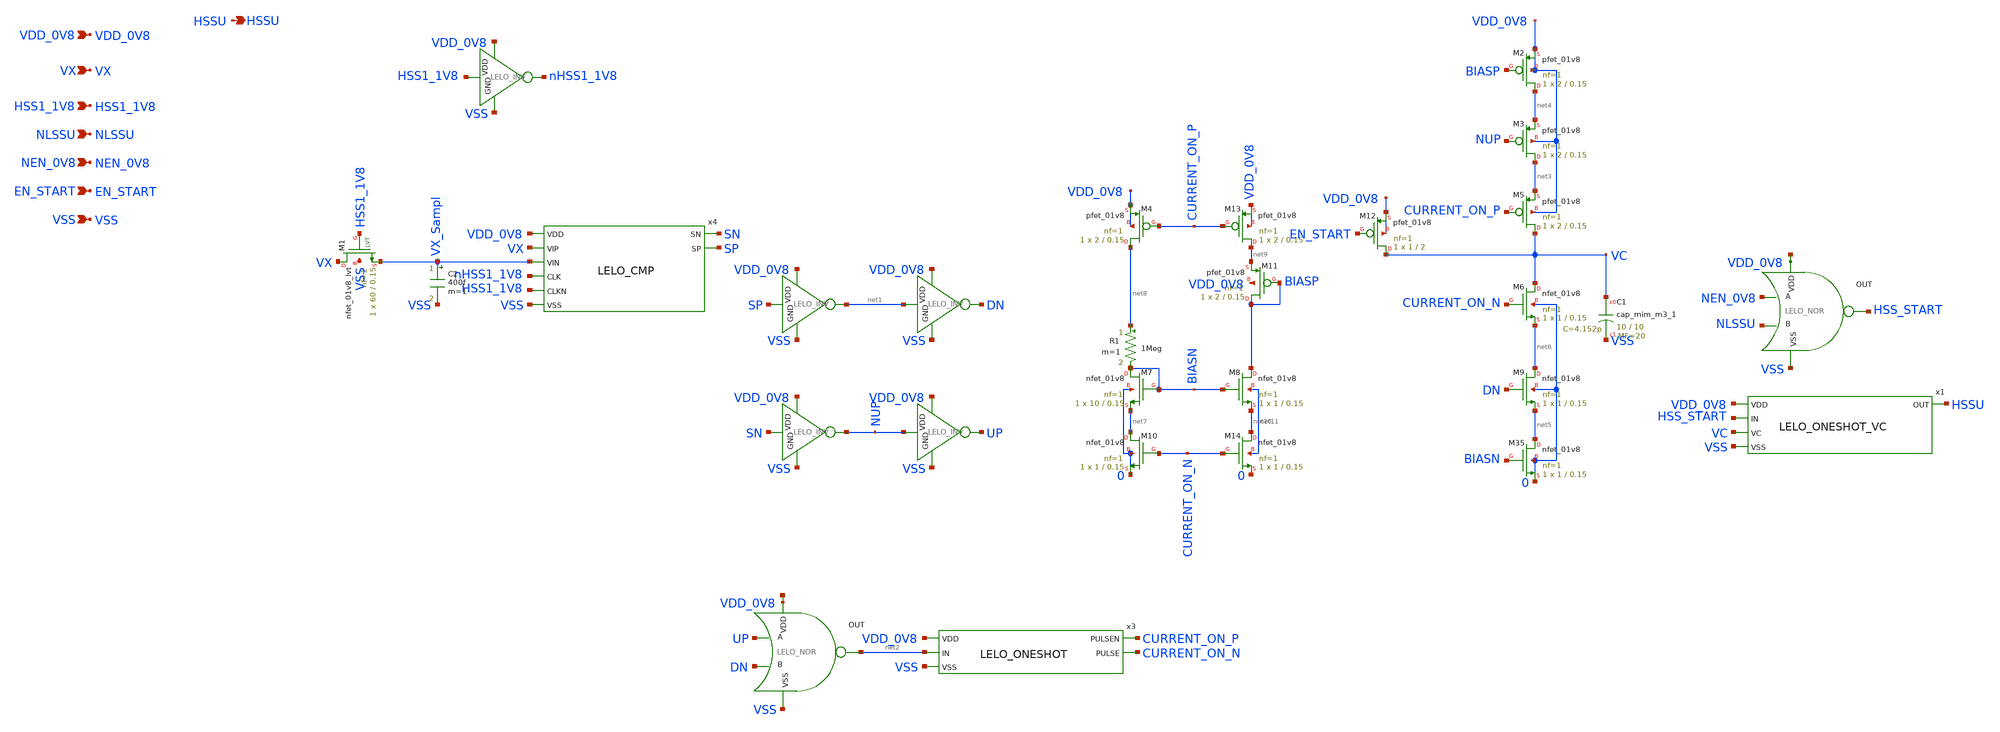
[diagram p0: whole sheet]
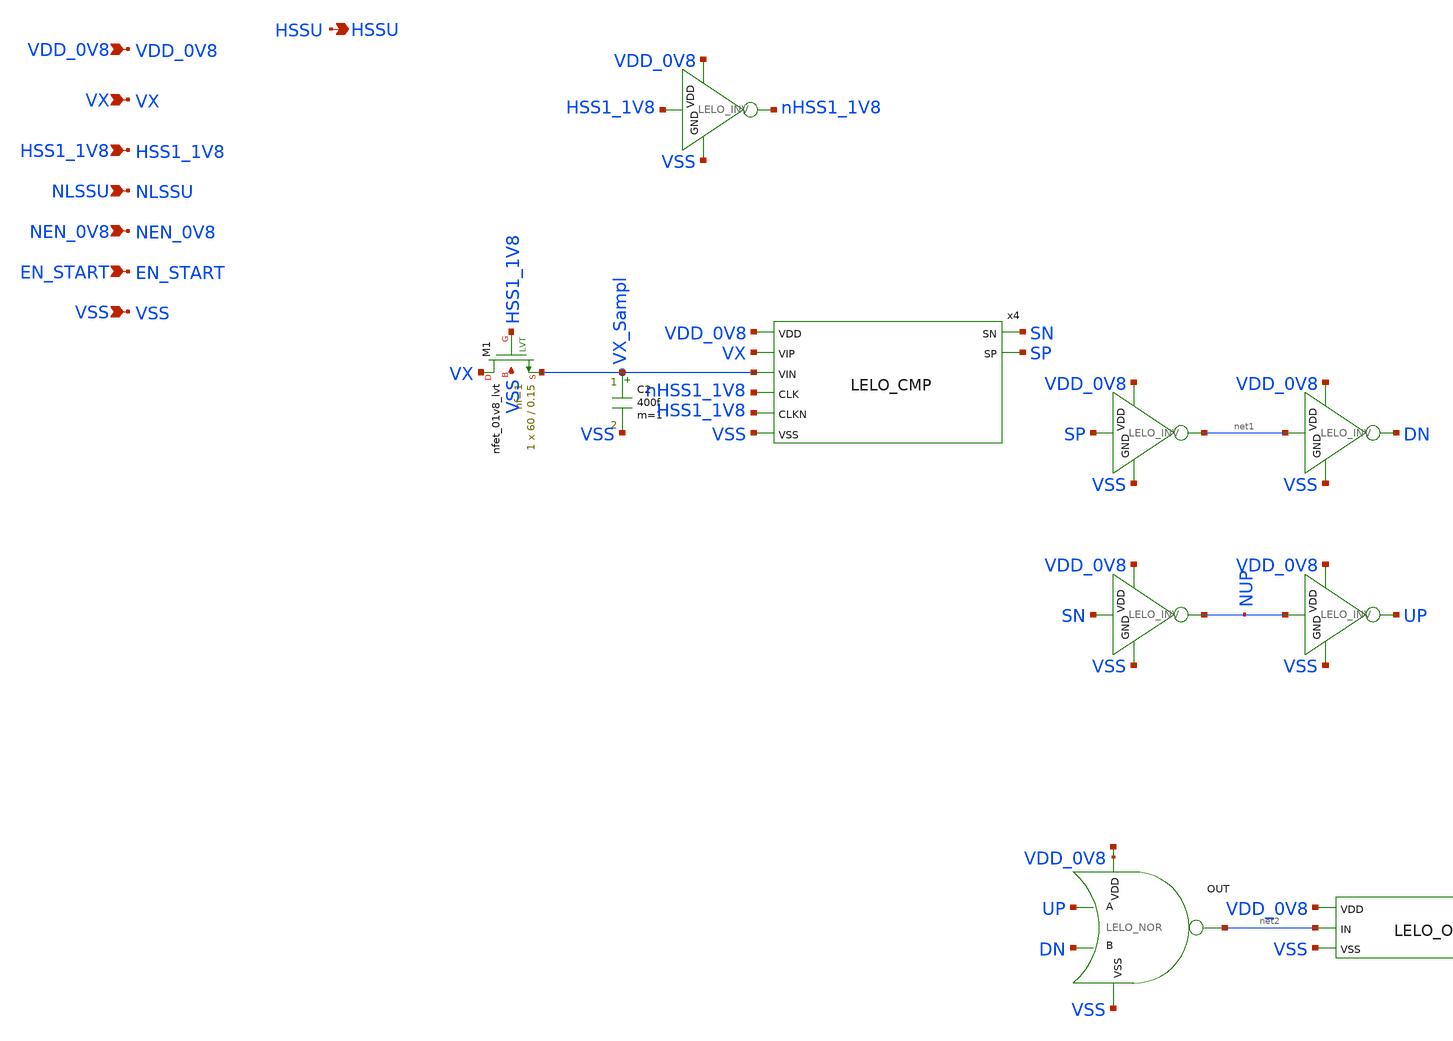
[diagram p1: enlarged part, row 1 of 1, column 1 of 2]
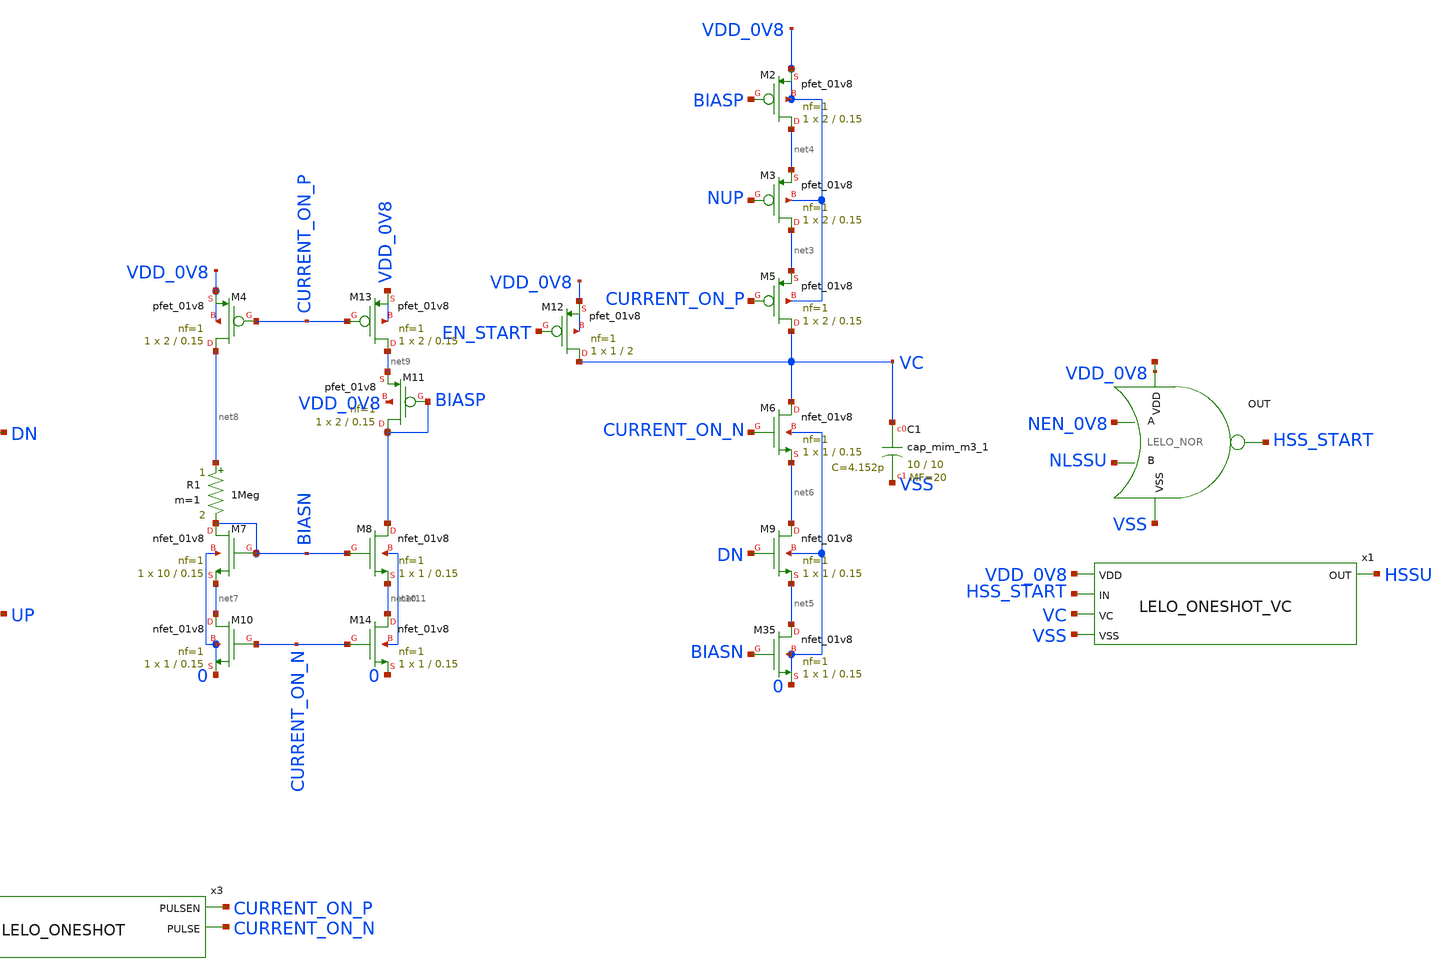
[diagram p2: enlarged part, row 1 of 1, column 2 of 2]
** sch_path: design/LELO_SVOD_SKY130A/LELO_SVOD_HSSCNTRL.sch
**.subckt LELO_SVOD_HSSCNTRL HSSU VX NLSSU VSS NEN_0V8 HSS1_1V8 VDD_0V8 EN_START
*.opin HSSU
*.ipin VX
*.ipin NLSSU
*.ipin VSS
*.ipin NEN_0V8
*.ipin HSS1_1V8
*.ipin VDD_0V8
*.ipin EN_START
x4 SN SP VDD_0V8 VX VX_Sampl nHSS1_1V8 HSS1_1V8 VSS LELO_CMP
x10 VDD_0V8 SP net1 VSS LELO_INV
x11 VDD_0V8 SN NUP VSS LELO_INV
x14 VDD_0V8 NUP UP VSS LELO_INV
x17 VDD_0V8 net1 DN VSS LELO_INV
x2 net12 net2 UP DN VSS LELO_NOR
x3 VDD_0V8 net2 VSS CURRENT_ON_P CURRENT_ON_N LELO_ONESHOT
x1 VDD_0V8 HSS_START VC HSSU VSS LELO_ONESHOT_VC
C2 VX_Sampl VSS 400f m=1
XM1 VX HSS1_1V8 VX_Sampl VSS sky130_fd_pr__nfet_01v8_lvt L=0.15 W=60 nf=1 ad='int((1 + 1)/2) * 60 / 1 * 0.29'
+ as='int((1 + 2)/2) * 60 / 1 * 0.29' pd='2*int((1 + 1)/2) * (60 / 1 + 0.29)' ps='2*int((1 + 2)/2) * (60 / 1 + 0.29)'
+ nrd='0.29 / 60 ' nrs='0.29 / 60 ' sa=0 sb=0 sd=0 mult=1 m=1
x5 VDD_0V8 HSS1_1V8 nHSS1_1V8 VSS LELO_INV
x6 net13 HSS_START NEN_0V8 NLSSU VSS LELO_NOR
XC1 VC VSS sky130_fd_pr__cap_mim_m3_1 W=10 L=10 MF=20 m=20
XM2 net4 BIASP VDD_0V8 VDD_0V8 sky130_fd_pr__pfet_01v8 L=0.15 W=2 nf=1 ad='int((1 + 1)/2) * 2 / 1 * 0.29'
+ as='int((1 + 2)/2) * 2 / 1 * 0.29' pd='2*int((1 + 1)/2) * (2 / 1 + 0.29)' ps='2*int((1 + 2)/2) * (2 / 1 + 0.29)'
+ nrd='0.29 / 2 ' nrs='0.29 / 2 ' sa=0 sb=0 sd=0 mult=1 m=1
XM3 net3 NUP net4 VDD_0V8 sky130_fd_pr__pfet_01v8 L=0.15 W=2 nf=1 ad='int((1 + 1)/2) * 2 / 1 * 0.29'
+ as='int((1 + 2)/2) * 2 / 1 * 0.29' pd='2*int((1 + 1)/2) * (2 / 1 + 0.29)' ps='2*int((1 + 2)/2) * (2 / 1 + 0.29)'
+ nrd='0.29 / 2 ' nrs='0.29 / 2 ' sa=0 sb=0 sd=0 mult=1 m=1
XM9 net6 DN net5 0 sky130_fd_pr__nfet_01v8 L=0.15 W=1 nf=1 ad='int((1 + 1)/2) * 1 / 1 * 0.29' as='int((1 + 2)/2) * 1 / 1 * 0.29'
+ pd='2*int((1 + 1)/2) * (1 / 1 + 0.29)' ps='2*int((1 + 2)/2) * (1 / 1 + 0.29)' nrd='0.29 / 1 ' nrs='0.29 / 1 '
+ sa=0 sb=0 sd=0 mult=1 m=1
XM35 net5 BIASN 0 0 sky130_fd_pr__nfet_01v8 L=0.15 W=1 nf=1 ad='int((1 + 1)/2) * 1 / 1 * 0.29' as='int((1 + 2)/2) * 1 / 1 * 0.29'
+ pd='2*int((1 + 1)/2) * (1 / 1 + 0.29)' ps='2*int((1 + 2)/2) * (1 / 1 + 0.29)' nrd='0.29 / 1 ' nrs='0.29 / 1 '
+ sa=0 sb=0 sd=0 mult=1 m=1
XM5 VC CURRENT_ON_P net3 VDD_0V8 sky130_fd_pr__pfet_01v8 L=0.15 W=2 nf=1 ad='int((1 + 1)/2) * 2 / 1 * 0.29'
+ as='int((1 + 2)/2) * 2 / 1 * 0.29' pd='2*int((1 + 1)/2) * (2 / 1 + 0.29)' ps='2*int((1 + 2)/2) * (2 / 1 + 0.29)'
+ nrd='0.29 / 2 ' nrs='0.29 / 2 ' sa=0 sb=0 sd=0 mult=1 m=1
XM6 VC CURRENT_ON_N net6 0 sky130_fd_pr__nfet_01v8 L=0.15 W=1 nf=1 ad='int((1 + 1)/2) * 1 / 1 * 0.29'
+ as='int((1 + 2)/2) * 1 / 1 * 0.29' pd='2*int((1 + 1)/2) * (1 / 1 + 0.29)' ps='2*int((1 + 2)/2) * (1 / 1 + 0.29)'
+ nrd='0.29 / 1 ' nrs='0.29 / 1 ' sa=0 sb=0 sd=0 mult=1 m=1
R1 net8 BIASN 1Meg m=1
XM7 BIASN BIASN net7 0 sky130_fd_pr__nfet_01v8 L=0.15 W=10 nf=1 ad='int((1 + 1)/2) * 10 / 1 * 0.29' as='int((1 + 2)/2) * 10 / 1 * 0.29'
+ pd='2*int((1 + 1)/2) * (10 / 1 + 0.29)' ps='2*int((1 + 2)/2) * (10 / 1 + 0.29)' nrd='0.29 / 10 ' nrs='0.29 / 10 '
+ sa=0 sb=0 sd=0 mult=1 m=1
XM8 BIASP BIASN net10 net11 sky130_fd_pr__nfet_01v8 L=0.15 W=1 nf=1 ad='int((1 + 1)/2) * 1 / 1 * 0.29'
+ as='int((1 + 2)/2) * 1 / 1 * 0.29' pd='2*int((1 + 1)/2) * (1 / 1 + 0.29)' ps='2*int((1 + 2)/2) * (1 / 1 + 0.29)'
+ nrd='0.29 / 1 ' nrs='0.29 / 1 ' sa=0 sb=0 sd=0 mult=1 m=1
XM10 net7 CURRENT_ON_N 0 0 sky130_fd_pr__nfet_01v8 L=0.15 W=1 nf=1 ad='int((1 + 1)/2) * 1 / 1 * 0.29'
+ as='int((1 + 2)/2) * 1 / 1 * 0.29' pd='2*int((1 + 1)/2) * (1 / 1 + 0.29)' ps='2*int((1 + 2)/2) * (1 / 1 + 0.29)'
+ nrd='0.29 / 1 ' nrs='0.29 / 1 ' sa=0 sb=0 sd=0 mult=1 m=1
XM11 BIASP BIASP net9 VDD_0V8 sky130_fd_pr__pfet_01v8 L=0.15 W=2 nf=1 ad='int((1 + 1)/2) * 2 / 1 * 0.29'
+ as='int((1 + 2)/2) * 2 / 1 * 0.29' pd='2*int((1 + 1)/2) * (2 / 1 + 0.29)' ps='2*int((1 + 2)/2) * (2 / 1 + 0.29)'
+ nrd='0.29 / 2 ' nrs='0.29 / 2 ' sa=0 sb=0 sd=0 mult=1 m=1
XM12 VC EN_START VDD_0V8 VDD_0V8 sky130_fd_pr__pfet_01v8 L=2 W=1 nf=1 ad='int((1 + 1)/2) * 1 / 1 * 0.29'
+ as='int((1 + 2)/2) * 1 / 1 * 0.29' pd='2*int((1 + 1)/2) * (1 / 1 + 0.29)' ps='2*int((1 + 2)/2) * (1 / 1 + 0.29)'
+ nrd='0.29 / 1 ' nrs='0.29 / 1 ' sa=0 sb=0 sd=0 mult=1 m=1
XM4 net8 CURRENT_ON_P VDD_0V8 VDD_0V8 sky130_fd_pr__pfet_01v8 L=0.15 W=2 nf=1 ad='int((1 + 1)/2) * 2 / 1 * 0.29'
+ as='int((1 + 2)/2) * 2 / 1 * 0.29' pd='2*int((1 + 1)/2) * (2 / 1 + 0.29)' ps='2*int((1 + 2)/2) * (2 / 1 + 0.29)'
+ nrd='0.29 / 2 ' nrs='0.29 / 2 ' sa=0 sb=0 sd=0 mult=1 m=1
XM13 net9 CURRENT_ON_P VDD_0V8 VDD_0V8 sky130_fd_pr__pfet_01v8 L=0.15 W=2 nf=1 ad='int((1 + 1)/2) * 2 / 1 * 0.29'
+ as='int((1 + 2)/2) * 2 / 1 * 0.29' pd='2*int((1 + 1)/2) * (2 / 1 + 0.29)' ps='2*int((1 + 2)/2) * (2 / 1 + 0.29)'
+ nrd='0.29 / 2 ' nrs='0.29 / 2 ' sa=0 sb=0 sd=0 mult=1 m=1
XM14 net10 CURRENT_ON_N 0 net11 sky130_fd_pr__nfet_01v8 L=0.15 W=1 nf=1 ad='int((1 + 1)/2) * 1 / 1 * 0.29'
+ as='int((1 + 2)/2) * 1 / 1 * 0.29' pd='2*int((1 + 1)/2) * (1 / 1 + 0.29)' ps='2*int((1 + 2)/2) * (1 / 1 + 0.29)'
+ nrd='0.29 / 1 ' nrs='0.29 / 1 ' sa=0 sb=0 sd=0 mult=1 m=1
**.ends
.end
